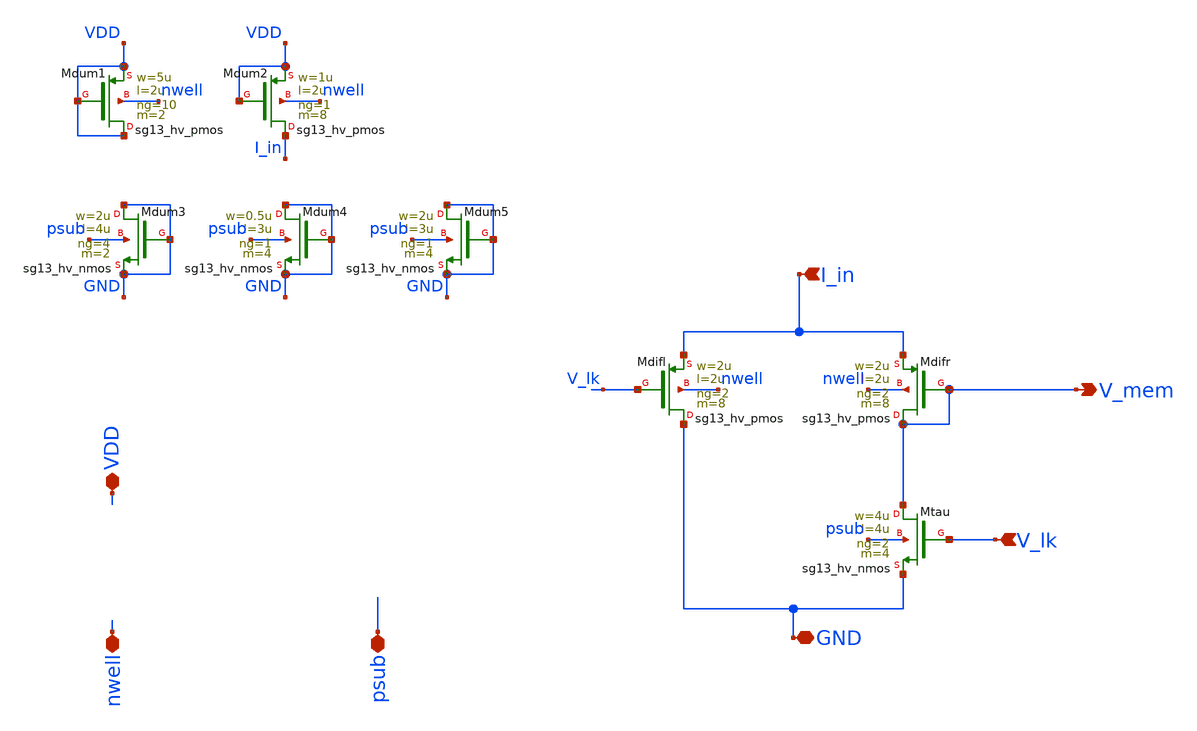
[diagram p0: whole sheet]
** sch_path: xschem/DPI.sch
**.subckt DPI V_mem V_lk I_in VDD GND nwell psub
*.opin V_mem
*.ipin V_lk
*.ipin I_in
*.iopin VDD
*.iopin GND
*.iopin nwell
*.iopin psub
XMdifl GND V_lk I_in nwell sg13_hv_pmos w=2u l=2u ng=2 m=8 mm_ok=1
XMdifr V_mem V_mem I_in nwell sg13_hv_pmos w=2u l=2u ng=2 m=8 mm_ok=1
XMtau V_mem V_lk GND psub sg13_hv_nmos w=4u l=4u ng=2 m=4 mm_ok=1
XMdum1 VDD VDD VDD nwell sg13_hv_pmos w=5u l=2u ng=10 m=2 mm_ok=1
XMdum2 I_in VDD VDD nwell sg13_hv_pmos w=1u l=2u ng=1 m=8 mm_ok=1
XMdum3 GND GND GND psub sg13_hv_nmos w=2u l=4u ng=4 m=2 mm_ok=1
XMdum4 GND GND GND psub sg13_hv_nmos w=0.5u l=3u ng=1 m=4 mm_ok=1
XMdum5 GND GND GND psub sg13_hv_nmos w=2u l=3u ng=1 m=4 mm_ok=1
**.ends
.end
